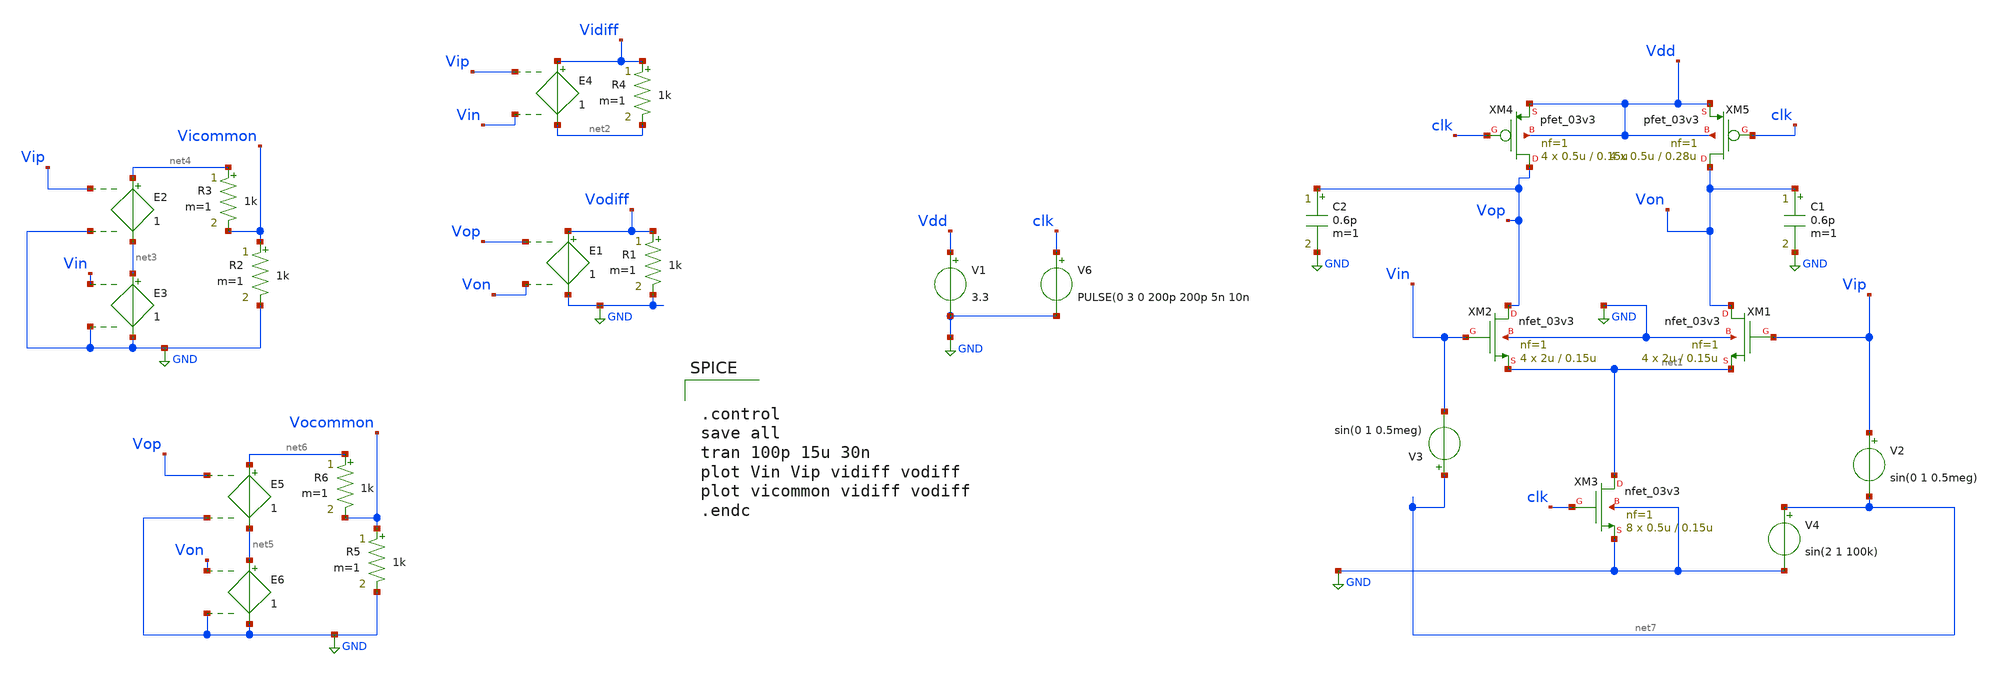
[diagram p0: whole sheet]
** sch_path: preamp/strongarm_preamp_dynamic_bulk_grounded_cap.sch
**.subckt strongarm_preamp_dynamic_bulk_grounded_cap
R4 Vidiff net2 1k m=1
E4 Vidiff net2 Vip Vin 1
R1 Vodiff GND 1k m=1
E1 Vodiff GND Vop Von 1
V6 clk GND PULSE(0 3 0 200p 200p 5n 10n
V2 Vip net7 sin(0 1 0.5meg)
E2 net4 net3 Vip GND 1
E3 net3 GND Vin GND 1
R2 Vicommon GND 1k m=1
R3 net4 Vicommon 1k m=1
E5 net6 net5 Vop GND 1
E6 net5 GND Von GND 1
R5 Vocommon GND 1k m=1
R6 net6 Vocommon 1k m=1
V1 Vdd GND 3.3
V4 net7 GND sin(2 1 100k)
V3 net7 Vin sin(0 1 0.5meg)
C1 Von GND 0.6p m=1
C2 Vop GND 0.6p m=1
XM1 Von Vip net1 GND nfet_03v3 L=0.15u W=2u nf=1 ad='int((nf+1)/2) * W/nf * 0.18u' as='int((nf+2)/2) * W/nf * 0.18u'
+ pd='2*int((nf+1)/2) * (W/nf + 0.18u)' ps='2*int((nf+2)/2) * (W/nf + 0.18u)' nrd='0.18u / W' nrs='0.18u / W'
+ sa=0 sb=0 sd=0 m=4
XM2 Vop Vin net1 GND nfet_03v3 L=0.15u W=2u nf=1 ad='int((nf+1)/2) * W/nf * 0.18u' as='int((nf+2)/2) * W/nf * 0.18u'
+ pd='2*int((nf+1)/2) * (W/nf + 0.18u)' ps='2*int((nf+2)/2) * (W/nf + 0.18u)' nrd='0.18u / W' nrs='0.18u / W'
+ sa=0 sb=0 sd=0 m=4
XM3 net1 clk GND GND nfet_03v3 L=0.15u W=0.5u nf=1 ad='int((nf+1)/2) * W/nf * 0.18u' as='int((nf+2)/2) * W/nf * 0.18u'
+ pd='2*int((nf+1)/2) * (W/nf + 0.18u)' ps='2*int((nf+2)/2) * (W/nf + 0.18u)' nrd='0.18u / W' nrs='0.18u / W'
+ sa=0 sb=0 sd=0 m=8
XM4 Vop clk Vdd Vdd pfet_03v3 L=0.15u W=0.5u nf=1 ad='int((nf+1)/2) * W/nf * 0.18u' as='int((nf+2)/2) * W/nf * 0.18u'
+ pd='2*int((nf+1)/2) * (W/nf + 0.18u)' ps='2*int((nf+2)/2) * (W/nf + 0.18u)' nrd='0.18u / W' nrs='0.18u / W'
+ sa=0 sb=0 sd=0 m=4
XM5 Von clk Vdd Vdd pfet_03v3 L=0.28u W=0.5u nf=1 ad='int((nf+1)/2) * W/nf * 0.18u' as='int((nf+2)/2) * W/nf * 0.18u'
+ pd='2*int((nf+1)/2) * (W/nf + 0.18u)' ps='2*int((nf+2)/2) * (W/nf + 0.18u)' nrd='0.18u / W' nrs='0.18u / W'
+ sa=0 sb=0 sd=0 m=4
**** begin user architecture code

.include /foss/pdks/gf180mcuC/libs.tech/ngspice/design.ngspice
.lib /foss/pdks/gf180mcuC/libs.tech/ngspice/sm141064.ngspice typical



.control
save all
tran 100p 15u 30n
plot Vin Vip vidiff vodiff
plot vicommon vidiff vodiff
.endc

**** end user architecture code
**.ends
.GLOBAL GND
.end
